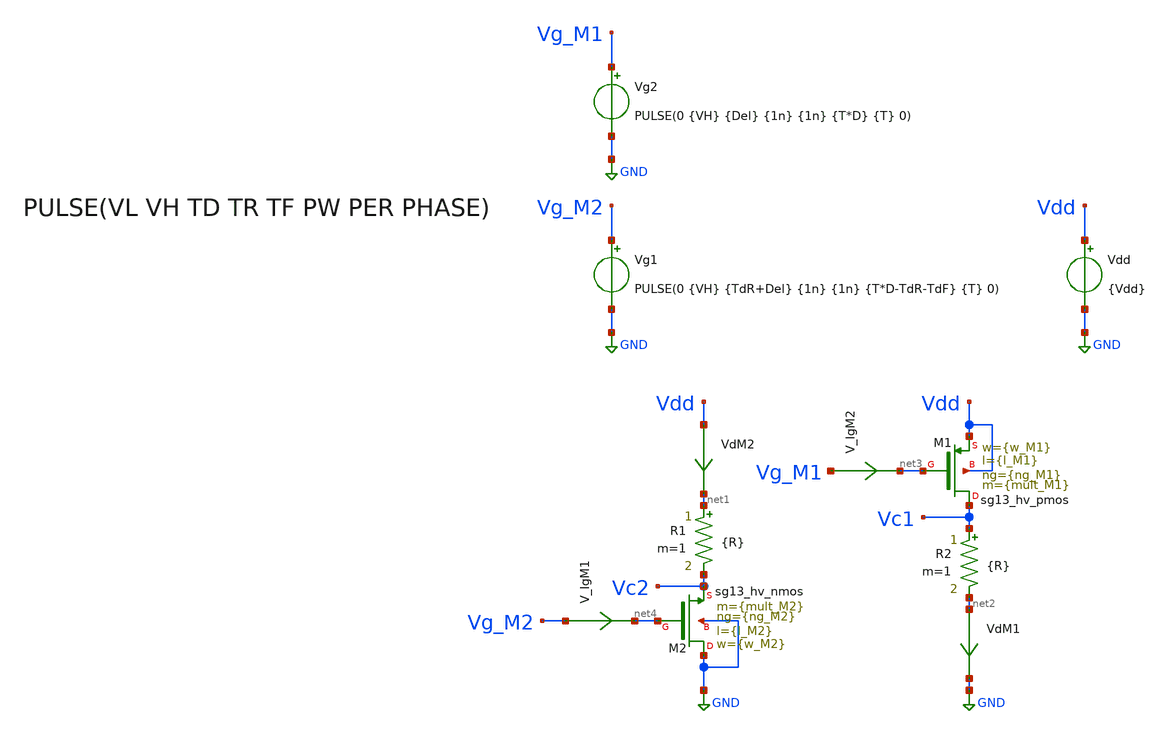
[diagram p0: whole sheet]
** sch_path: Tarea_1/xschem/TB_hvMOS_switch_test_IPD413_202501_HW1.sch
**.subckt TB_hvMOS_switch_test_IPD413_202501_HW1
XM2 GND net4 Vc2 GND sg13_hv_nmos w={w_M2} l={l_M2} ng={ng_M2} m={mult_M2} mm_ok=1
XM1 Vc1 net3 Vdd Vdd sg13_hv_pmos w={w_M1} l={l_M1} ng={ng_M1} m={mult_M1} mm_ok=1
Vdd Vdd GND {Vdd}
VdM2 Vdd net1 0
.save i(vdm2)
VdM1 net2 GND 0
.save i(vdm1)
Vg1 Vg_M2 GND PULSE(0 {VH} {TdR+Del} {1n} {1n} {T*D-TdR-TdF} {T} 0)
Vg2 Vg_M1 GND PULSE(0 {VH} {Del} {1n} {1n} {T*D} {T} 0)
R1 net1 Vc2 {R} m=1
R2 Vc1 net2 {R} m=1
V_IgM1 Vg_M2 net4 0
.save i(v_igm1)
V_IgM2 Vg_M1 net3 0
.save i(v_igm2)
**** begin user architecture code

.lib cornerMOShv.lib mos_tt




.param Vdd = 3.3
.param VH = 3.3
.param V_on = 330m
.param I_on = 2

.param f_sw = 1Meg
.param D = 0.5
.param T = 1/f_sw
.param TR = T*0.01
.param TF = T*0.01
.param Del = 0.05u
* Tiempos muertos
.param TdR = 1n
.param TdF = 1n

.param R = (Vdd - V_on)/I_on

.param temp = 27







.save all
.param SimTime = 10*T

.tran 1n {SimTime}
.control
reset
set color0 = white
*tran 1n 1u
run
let VsdM1 = v(Vdd) - v(Vc1)
let VdsM2 = v(Vc2)
plot i(VdM1) i(VdM2)
plot v(Vc1) v(Vc2)
plot v(Vg_M1) v(Vg_M2)
plot VsdM1 VdsM2
plot i(V_IgM1) i(V_IgM2)
meas TRAN td_off_M1 TRIG v(Vg_M1) VAL=0.33 RISE=1 TARG VsdM1 VAL=0.33 RISE=1
meas TRAN td_on_M1 TRIG v(Vg_M1) VAL=2.97 FALL=1 TARG VsdM1 VAL=2.97 FALL=1
meas TRAN td_on_M2 TRIG v(Vg_M2) VAL=0.33 RISE=1 TARG VdsM2 VAL=2.97 FALL=1
meas TRAN td_off_M2 TRIG v(Vg_M2) VAL=2.97 FALL=1 TARG VdsM2 VAL=0.33 RISE=1
let TdR = td_off_M1 - td_on_M2
let TdF = td_on_M1 - td_off_M2
print TdR TdF
wrdata switch_test.raw V(Vc1) i(VdM1) V(Vc2) i(VdM2)
.endc

.end




.param temp=27
.param global_mult = {1024}
.param mult_M1 = {3*global_mult}
.param w_M1 =10u
.param l_M1 = 0.4u
.param ng_M1 = 1

.param mult_M2 = {1*global_mult}
.param w_M2 =10u
.param l_M2 =0.45u
.param ng_M2 =1





**** end user architecture code
**.ends
.GLOBAL GND
.end
